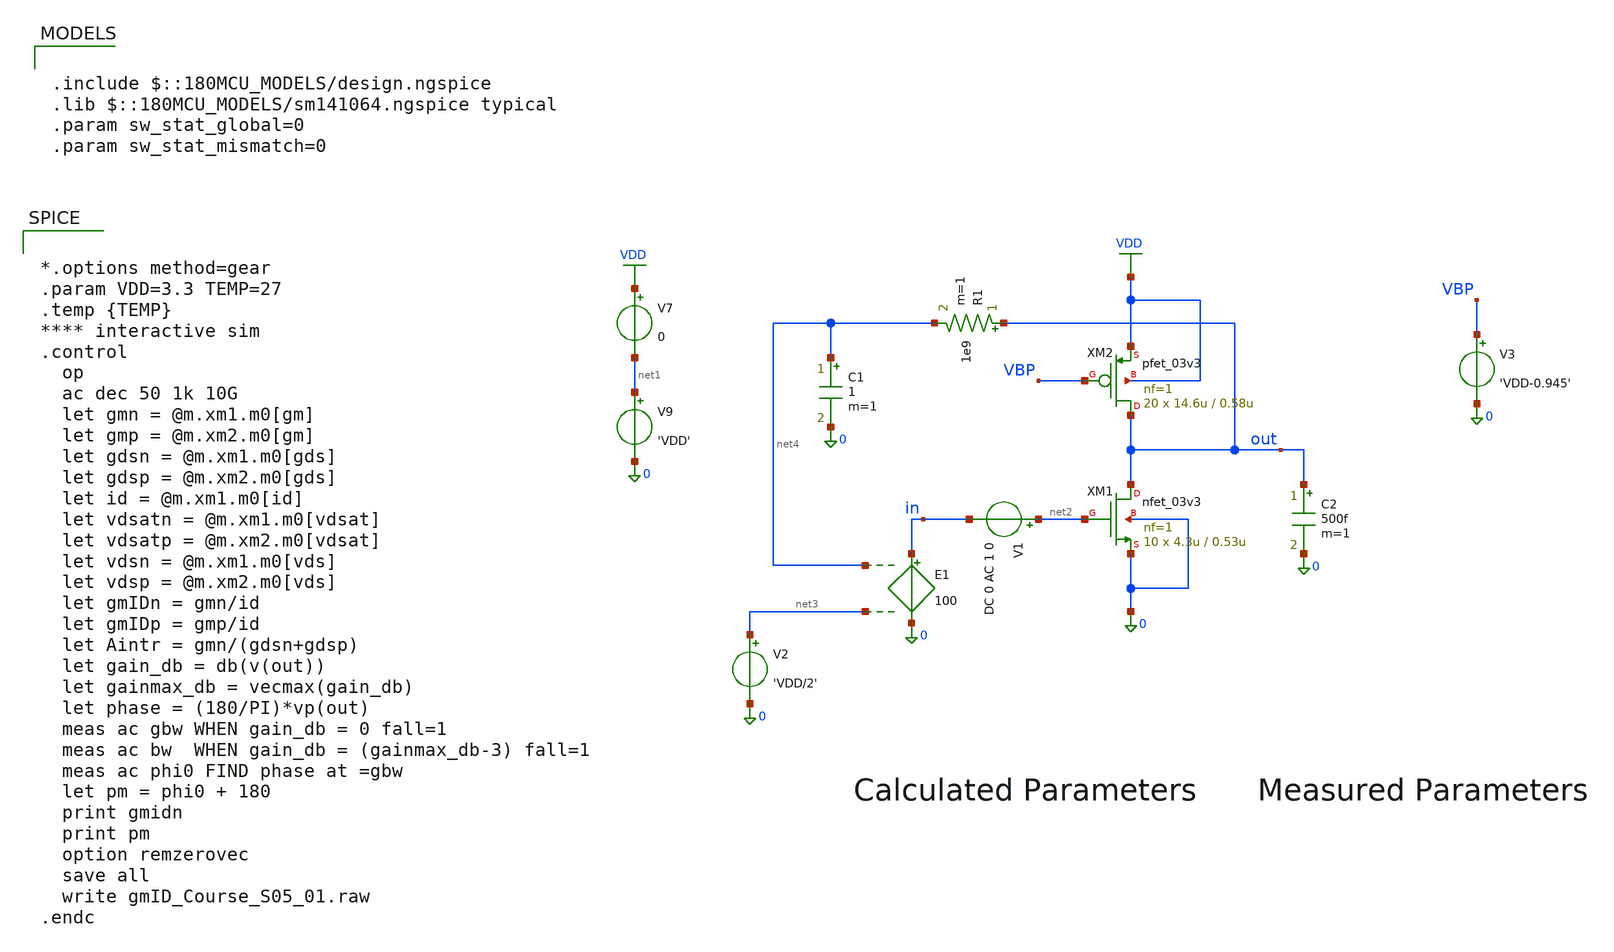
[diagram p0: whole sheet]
** sch_path: Xschem/gf180mcuD/gmID_Designs/gmID_Course_S05_01.sch
**.subckt gmID_Course_S05_01
XM1 out net2 0 0 nfet_03v3 L=0.53u W=4.3u nf=1 ad='int((nf+1)/2) * W/nf * 0.18u' as='int((nf+2)/2) * W/nf * 0.18u'
+ pd='2*int((nf+1)/2) * (W/nf + 0.18u)' ps='2*int((nf+2)/2) * (W/nf + 0.18u)' nrd='0.18u / W' nrs='0.18u / W'
+ sa=0 sb=0 sd=0 m=10
E1 in 0 net4 net3 100
R1 out net4 1e9 m=1
C1 net4 0 1 m=1
V1 net2 in DC 0 AC 1 0
V9 net1 0 'VDD'
V7 VDD net1 0
C2 out 0 500f m=1
V2 net3 0 'VDD/2'
XM2 out VBP VDD VDD pfet_03v3 L=0.58u W=14.6u nf=1 ad='int((nf+1)/2) * W/nf * 0.18u' as='int((nf+2)/2) * W/nf * 0.18u'
+ pd='2*int((nf+1)/2) * (W/nf + 0.18u)' ps='2*int((nf+2)/2) * (W/nf + 0.18u)' nrd='0.18u / W' nrs='0.18u / W'
+ sa=0 sb=0 sd=0 m=20
V3 VBP 0 'VDD-0.945'
**** begin user architecture code

.include $::180MCU_MODELS/design.ngspice
.lib $::180MCU_MODELS/sm141064.ngspice typical
.param sw_stat_global=0
.param sw_stat_mismatch=0



*.options method=gear
.param VDD=3.3 TEMP=27
.temp {TEMP}
**** interactive sim
.control
  op
  ac dec 50 1k 10G
  let gmn = @m.xm1.m0[gm]
  let gmp = @m.xm2.m0[gm]
  let gdsn = @m.xm1.m0[gds]
  let gdsp = @m.xm2.m0[gds]
  let id = @m.xm1.m0[id]
  let vdsatn = @m.xm1.m0[vdsat]
  let vdsatp = @m.xm2.m0[vdsat]
  let vdsn = @m.xm1.m0[vds]
  let vdsp = @m.xm2.m0[vds]
  let gmIDn = gmn/id
  let gmIDp = gmp/id
  let Aintr = gmn/(gdsn+gdsp)
  let gain_db = db(v(out))
  let gainmax_db = vecmax(gain_db)
  let phase = (180/PI)*vp(out)
  meas ac gbw WHEN gain_db = 0 fall=1
  meas ac bw  WHEN gain_db = (gainmax_db-3) fall=1
  meas ac phi0 FIND phase at =gbw
  let pm = phi0 + 180
  print gmidn
  print pm
  option remzerovec
  save all
  write gmID_Course_S05_01.raw
.endc


**** end user architecture code
**.ends
.GLOBAL VDD
.end
